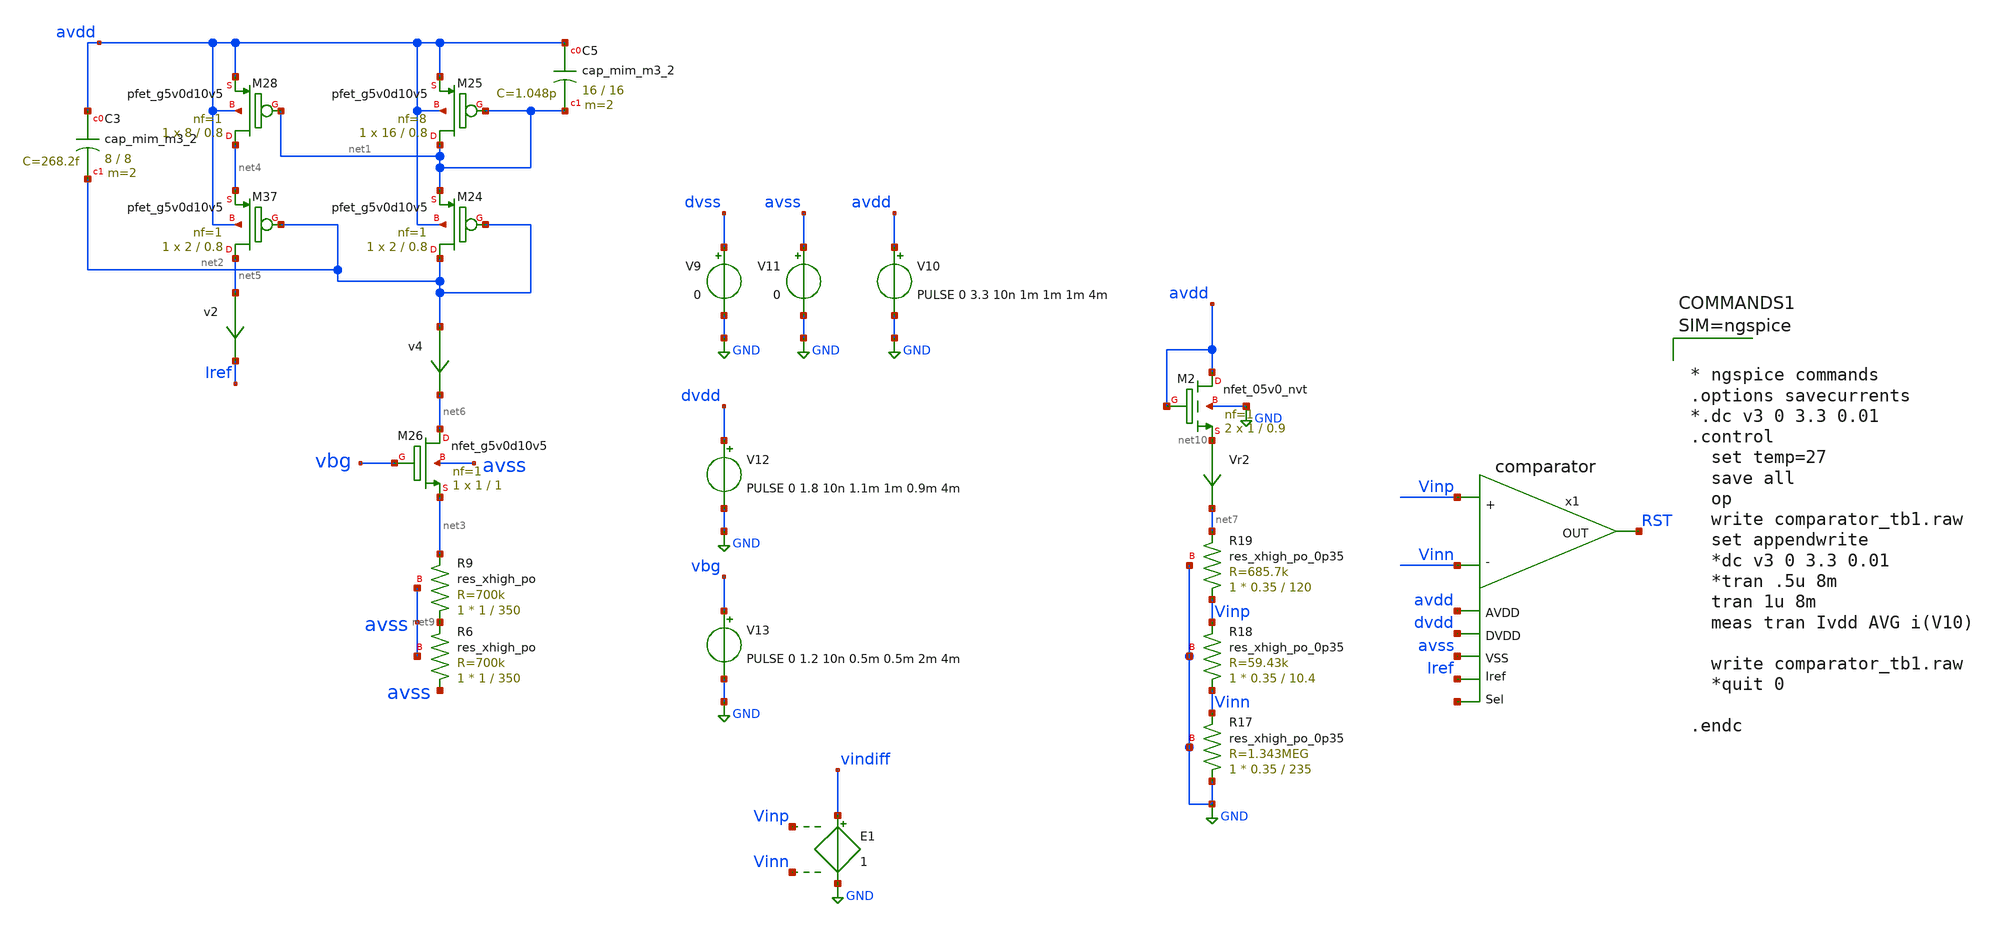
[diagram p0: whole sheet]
** sch_path: xschem_sim/comparator_tb1.sch
**.subckt comparator_tb1
x1 Iref Vinn Vinp RST avss avdd dvdd net8 comparator
V9 dvss GND 0
V10 avdd GND PULSE 0 3.3 10n 1m 1m 1m 4m
V11 avss GND 0
V12 dvdd GND PULSE 0 1.8 10n 1.1m 1m 0.9m 4m
V13 vbg GND PULSE 0 1.2 10n 0.5m 0.5m 2m 4m
v2 net5 Iref 0
.save i(v2)
XM24 net2 net2 net1 avdd sky130_fd_pr__pfet_g5v0d10v5 L=0.8 W=2 nf=1 ad='int((nf+1)/2) * W/nf * 0.29'
+ as='int((nf+2)/2) * W/nf * 0.29' pd='2*int((nf+1)/2) * (W/nf + 0.29)' ps='2*int((nf+2)/2) * (W/nf + 0.29)'
+ nrd='0.29 / W' nrs='0.29 / W' sa=0 sb=0 sd=0 mult=1 m=1
XM25 net1 net1 avdd avdd sky130_fd_pr__pfet_g5v0d10v5 L=0.8 W=16 nf=8 ad='int((nf+1)/2) * W/nf * 0.29'
+ as='int((nf+2)/2) * W/nf * 0.29' pd='2*int((nf+1)/2) * (W/nf + 0.29)' ps='2*int((nf+2)/2) * (W/nf + 0.29)'
+ nrd='0.29 / W' nrs='0.29 / W' sa=0 sb=0 sd=0 mult=1 m=1
XM26 net6 vbg net3 avss sky130_fd_pr__nfet_g5v0d10v5 L=1 W=1 nf=1 ad='int((nf+1)/2) * W/nf * 0.29' as='int((nf+2)/2) * W/nf * 0.29'
+ pd='2*int((nf+1)/2) * (W/nf + 0.29)' ps='2*int((nf+2)/2) * (W/nf + 0.29)' nrd='0.29 / W' nrs='0.29 / W'
+ sa=0 sb=0 sd=0 mult=1 m=1
XM28 net4 net1 avdd avdd sky130_fd_pr__pfet_g5v0d10v5 L=0.8 W=8 nf=1 ad='int((nf+1)/2) * W/nf * 0.29'
+ as='int((nf+2)/2) * W/nf * 0.29' pd='2*int((nf+1)/2) * (W/nf + 0.29)' ps='2*int((nf+2)/2) * (W/nf + 0.29)'
+ nrd='0.29 / W' nrs='0.29 / W' sa=0 sb=0 sd=0 mult=1 m=1
XM37 net5 net2 net4 avdd sky130_fd_pr__pfet_g5v0d10v5 L=0.8 W=2 nf=1 ad='int((nf+1)/2) * W/nf * 0.29'
+ as='int((nf+2)/2) * W/nf * 0.29' pd='2*int((nf+1)/2) * (W/nf + 0.29)' ps='2*int((nf+2)/2) * (W/nf + 0.29)'
+ nrd='0.29 / W' nrs='0.29 / W' sa=0 sb=0 sd=0 mult=1 m=1
v4 net2 net6 0
.save i(v4)
XC5 avdd net1 sky130_fd_pr__cap_mim_m3_2 W=16 L=16 MF=2 m=2
XC3 avdd net2 sky130_fd_pr__cap_mim_m3_2 W=8 L=8 MF=2 m=2
XR9 net9 net3 avss sky130_fd_pr__res_xhigh_po W=1 L=350 mult=1 m=1
XR6 avss net9 avss sky130_fd_pr__res_xhigh_po W=1 L=350 mult=1 m=1
Vr2 net10 net7 0
.save i(vr2)
XR17 GND Vinn GND sky130_fd_pr__res_xhigh_po_0p35 L=235 mult=1 m=1
XR18 Vinn Vinp GND sky130_fd_pr__res_xhigh_po_0p35 L=10.4 mult=1 m=1
XR19 Vinp net7 GND sky130_fd_pr__res_xhigh_po_0p35 L=120 mult=1 m=1
XM2 avdd avdd net10 GND sky130_fd_pr__nfet_05v0_nvt L=0.9 W=1 nf=1 ad='int((nf+1)/2) * W/nf * 0.29' as='int((nf+2)/2) * W/nf * 0.29'
+ pd='2*int((nf+1)/2) * (W/nf + 0.29)' ps='2*int((nf+2)/2) * (W/nf + 0.29)' nrd='0.29 / W' nrs='0.29 / W'
+ sa=0 sb=0 sd=0 mult=2 m=2
E1 vindiff GND Vinp Vinn 1
**** begin user architecture code



* ngspice commands
.options savecurrents
*.dc v3 0 3.3 0.01
.control
  set temp=27
  save all
  op
  write comparator_tb1.raw
  set appendwrite
  *dc v3 0 3.3 0.01
  *tran .5u 8m
  tran 1u 8m
  meas tran Ivdd AVG i(V10)

  write comparator_tb1.raw
  *quit 0

.endc



 .lib $::SKYWATER_MODELS/sky130.lib.spice tt

.include $::SKYWATER_STDCELLS/sky130_fd_sc_hd.spice
.include $::SKYWATER_STDCELLS/../../sky130_fd_sc_hvl/spice/sky130_fd_sc_hvl.spice


**** end user architecture code
**.ends
.GLOBAL GND
.end
